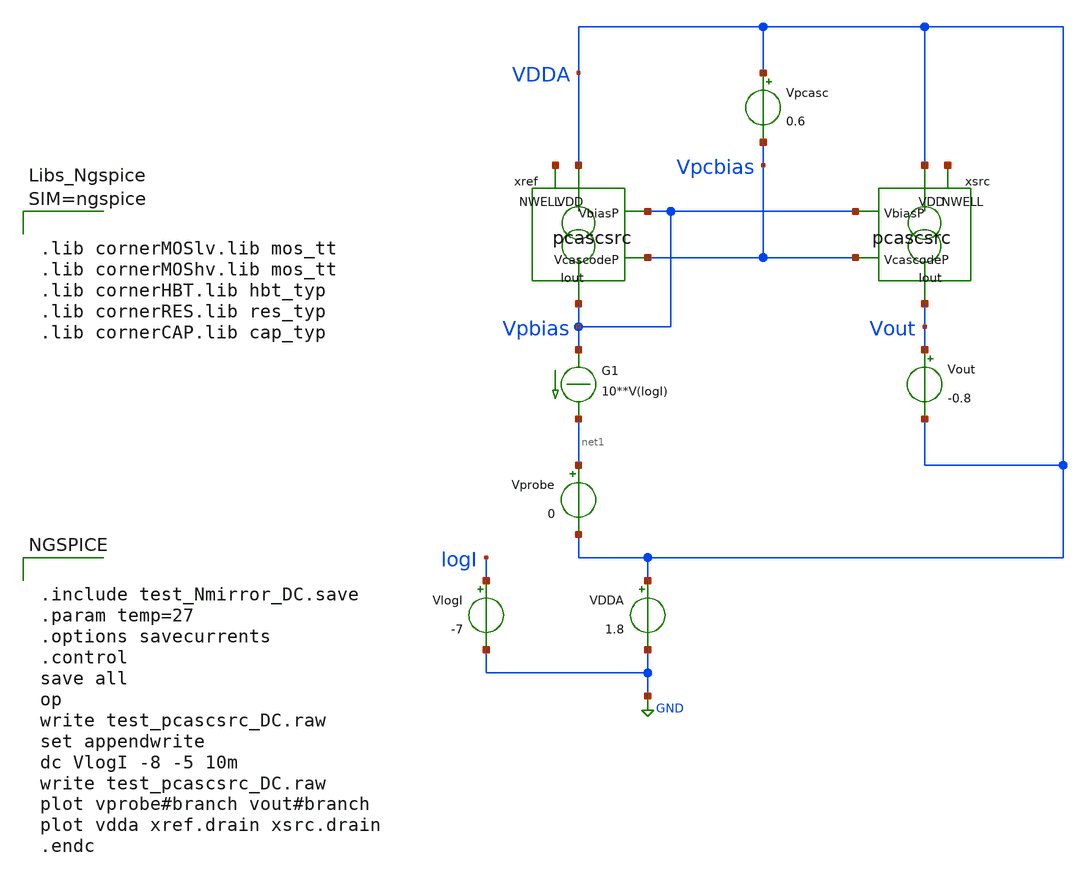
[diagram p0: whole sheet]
** sch_path: xschem/test_pcascsrc_DC.sch
**.subckt test_pcascsrc_DC
Vout Vout VDDA -0.8
.save i(vout)
Vprobe net1 VDDA 0
.save i(vprobe)
G1 Vpbias net1 CUR=' 10**V(logI) '
VlogI logI GND -7
.save i(vlogi)
xref VDDA Vpbias Vpcbias Vpbias net2 pcascsrc
xsrc VDDA Vpbias Vpcbias Vout net3 pcascsrc
VDDA VDDA GND 1.8
.save i(vdda)
Vpcasc VDDA Vpcbias 0.6
.save i(vpcasc)
**** begin user architecture code


.include test_Nmirror_DC.save
.param temp=27
.options savecurrents
.control
save all
op
write test_pcascsrc_DC.raw
set appendwrite
dc VlogI -8 -5 10m
write test_pcascsrc_DC.raw
plot vprobe#branch vout#branch
plot vdda xref.drain xsrc.drain
.endc





.lib cornerMOSlv.lib mos_tt
.lib cornerMOShv.lib mos_tt
.lib cornerHBT.lib hbt_typ
.lib cornerRES.lib res_typ
.lib cornerCAP.lib cap_typ



**** end user architecture code
**.ends

* expanding   symbol:  pcascsrc.sym # of pins=5
** sym_path: xschem/pcascsrc.sym
** sch_path: xschem/pcascsrc.sch
.subckt pcascsrc VDD VbiasP VcascodeP Iout NWELL
*.ipin VcascodeP
*.ipin VbiasP
*.opin Iout
*.ipin VDD
*.iopin NWELL
XMsrc drain VbiasP VDD NWELL sg13_lv_pmos w=0.74u l=2u ng=1 m=1 mm_ok=1
XMcasc Iout VcascodeP drain NWELL sg13_lv_pmos w=0.3u l=0.3u ng=1 m=1 mm_ok=1
.ends

.GLOBAL GND
.end
